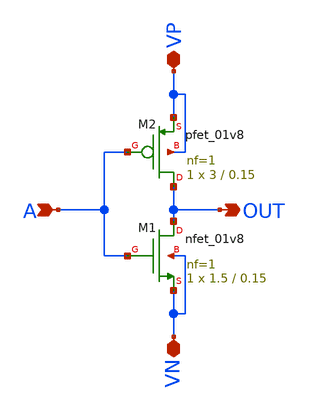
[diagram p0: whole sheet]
** sch_path: skywater_stuff/INV_VP_VN_LVS.sch
**.subckt INV_VP_VN_LVS A OUT VP VN
*.ipin A
*.opin OUT
*.iopin VP
*.iopin VN
XM1 OUT A VN VN sky130_fd_pr__nfet_01v8 L=0.15 W=1.5 nf=1 ad='int((nf+1)/2) * W/nf * 0.29' as='int((nf+2)/2) * W/nf * 0.29'
+ pd='2*int((nf+1)/2) * (W/nf + 0.29)' ps='2*int((nf+2)/2) * (W/nf + 0.29)' nrd='0.29 / W' nrs='0.29 / W'
+ sa=0 sb=0 sd=0 mult=1 m=1
XM2 OUT A VP VP sky130_fd_pr__pfet_01v8 L=0.15 W=3 nf=1 ad='int((nf+1)/2) * W/nf * 0.29' as='int((nf+2)/2) * W/nf * 0.29'
+ pd='2*int((nf+1)/2) * (W/nf + 0.29)' ps='2*int((nf+2)/2) * (W/nf + 0.29)' nrd='0.29 / W' nrs='0.29 / W'
+ sa=0 sb=0 sd=0 mult=1 m=1
**.ends
.end
